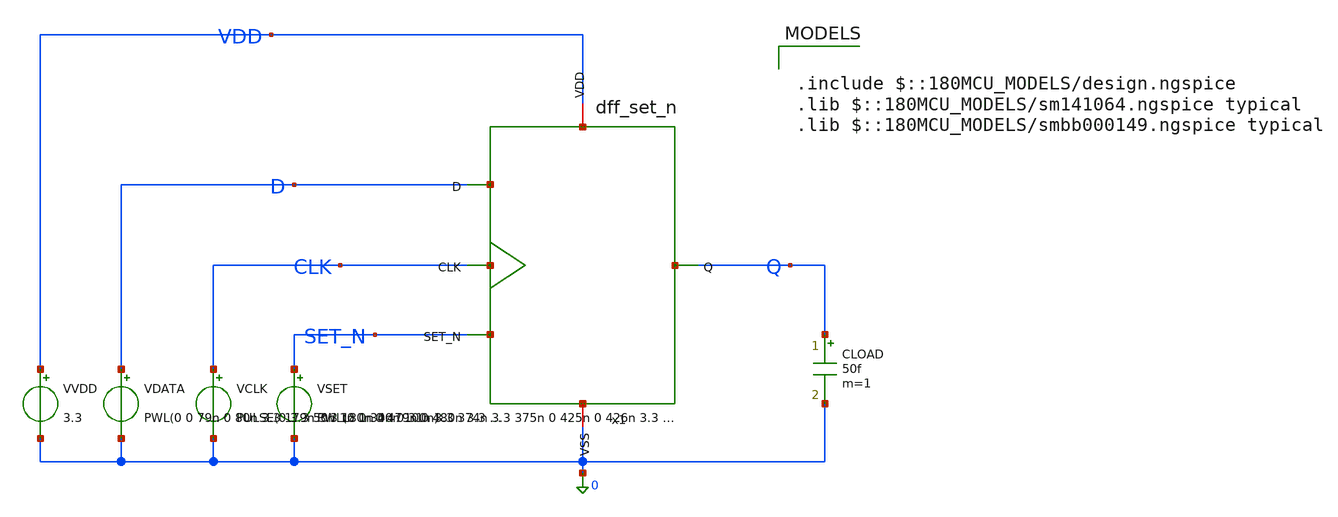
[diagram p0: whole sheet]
** sch_path: sar_logic/sar_designs/tb_dff_set_n.sch
**.subckt tb_dff_set_n
VSET SET_N 0 PWL(0 0 30n 0 31n 3.3 374n 3.3 375n 0 425n 0 426n 3.3 750n 3.3)
VCLK CLK 0 PULSE(0 3.3 50n 1n 1n 40n 100n)
VDATA D 0 PWL(0 0 79n 0 80n 3.3 179n 3.3 180n 0 479n 0 480n 3.3 579n 3.3 580n 0 750n 0)
VVDD VDD 0 3.3
CLOAD Q 0 50f m=1
x1 VDD CLK D Q SET_N 0 dff_set_n
**** begin user architecture code

.include $::180MCU_MODELS/design.ngspice
.lib $::180MCU_MODELS/sm141064.ngspice typical
.lib $::180MCU_MODELS/smbb000149.ngspice typical



.options method=gear reltol=1e-3 abstol=1e-12 vntol=1e-6

.control
  save all
  tran 10p 750n

  meas tran q020 FIND v(Q) AT=20n
  meas tran q070 FIND v(Q) AT=70n
  meas tran q120 FIND v(Q) AT=120n
  meas tran q170 FIND v(Q) AT=170n
  meas tran q220 FIND v(Q) AT=220n
  meas tran q270 FIND v(Q) AT=270n
  meas tran q370 FIND v(Q) AT=370n
  meas tran q385 FIND v(Q) AT=385n
  meas tran q415 FIND v(Q) AT=415n
  meas tran q440 FIND v(Q) AT=440n
  meas tran q470 FIND v(Q) AT=470n
  meas tran q570 FIND v(Q) AT=570n
  meas tran q670 FIND v(Q) AT=670n

  meas tran tcq_rise TRIG v(CLK) VAL=1.65 RISE=1 TD=100n
    TARG v(Q) VAL=1.65 RISE=1 TD=149n
  meas tran tcq_fall TRIG v(CLK) VAL=1.65 RISE=1 TD=200n
    TARG v(Q) VAL=1.65 FALL=1 TD=249n
  meas tran t_async_set TRIG v(SET_N) VAL=1.65 FALL=1 TD=370n
    TARG v(Q) VAL=1.65 RISE=1 TD=374n

  let failures = 0

  if q020 < 2.97
    echo FAIL_q020_preset_did_not_force_Q_high
    let failures = failures + 1
  end

  if q070 > 0.33
    echo FAIL_q070_Q_should_capture_low
    let failures = failures + 1
  end

  if q120 > 0.33
    echo FAIL_q120_Q_changed_before_rising_edge
    let failures = failures + 1
  end

  if q170 < 2.97
    echo FAIL_q170_Q_did_not_capture_high
    let failures = failures + 1
  end

  if q220 < 2.97
    echo FAIL_q220_Q_did_not_hold_high
    let failures = failures + 1
  end

  if q270 > 0.33
    echo FAIL_q270_Q_did_not_capture_low
    let failures = failures + 1
  end

  if q370 > 0.33
    echo FAIL_q370_Q_should_still_be_low
    let failures = failures + 1
  end

  if q385 < 2.97
    echo FAIL_q385_async_preset_did_not_force_Q_high
    let failures = failures + 1
  end

  if q415 < 2.97
    echo FAIL_q415_Q_did_not_remain_preset
    let failures = failures + 1
  end

  if q440 < 2.97
    echo FAIL_q440_Q_changed_immediately_after_preset_release
    let failures = failures + 1
  end

  if q470 > 0.33
    echo FAIL_q470_Q_should_capture_low
    let failures = failures + 1
  end

  if q570 < 2.97
    echo FAIL_q570_Q_should_capture_high
    let failures = failures + 1
  end

  if q670 > 0.33
    echo FAIL_q670_Q_should_capture_low
    let failures = failures + 1
  end

  echo
  echo MEASURED_DELAYS
  print tcq_rise tcq_fall t_async_set
  echo

  if failures < 0.5
    echo PASS_tb_dff_set_n_all_functional_checks_passed
  else
    echo FAIL_tb_dff_set_n
    print failures
  end

  write tb_dff_set_n.raw
  plot v(CLK) v(D) v(SET_N) v(Q)
.endc


**** end user architecture code
**.ends
.end
